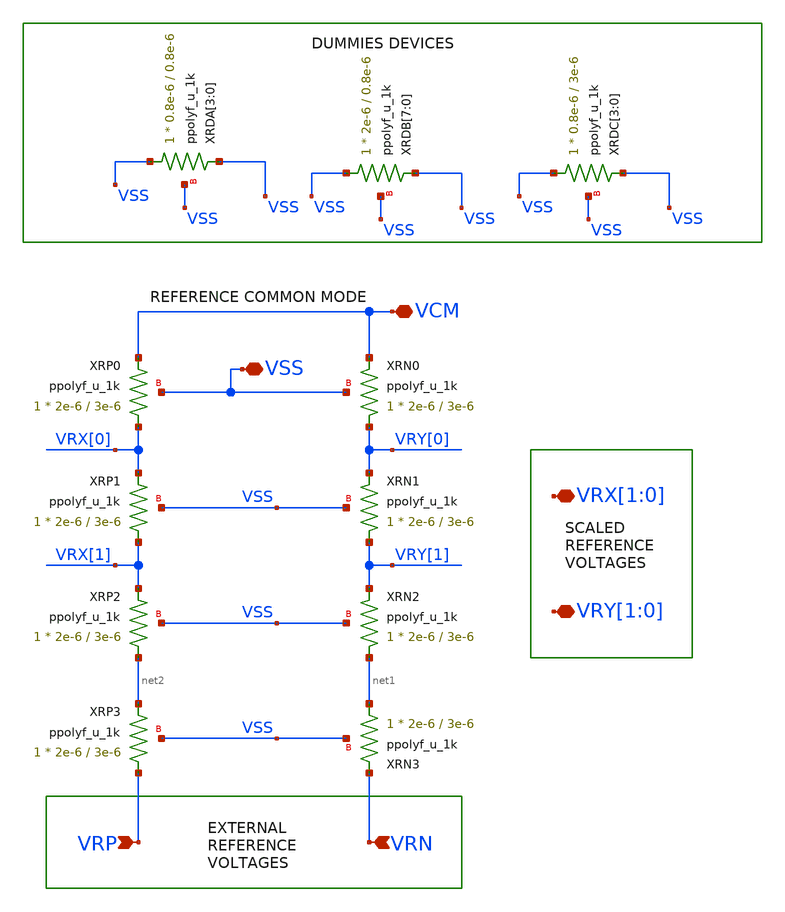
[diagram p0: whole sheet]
** sch_path: designs/sar_adc/dac/rdac/xschem/rdac.sch
**.subckt rdac VRN VRP VCM VRY[1],VRY[0] VRX[1],VRX[0] VSS
*.ipin VRN
*.ipin VRP
*.iopin VCM
*.iopin VRY[1],VRY[0]
*.iopin VRX[1],VRX[0]
*.iopin VSS
XRN0 VRY[0] VCM VSS ppolyf_u_1k r_width=2e-6 r_length=3e-6 m=1
XRN1 VRY[1] VRY[0] VSS ppolyf_u_1k r_width=2e-6 r_length=3e-6 m=1
XRN2 net1 VRY[1] VSS ppolyf_u_1k r_width=2e-6 r_length=3e-6 m=1
XRN3 net1 VRN VSS ppolyf_u_1k r_width=2e-6 r_length=3e-6 m=1
XRP0 VRX[0] VCM VSS ppolyf_u_1k r_width=2e-6 r_length=3e-6 m=1
XRP1 VRX[1] VRX[0] VSS ppolyf_u_1k r_width=2e-6 r_length=3e-6 m=1
XRP2 net2 VRX[1] VSS ppolyf_u_1k r_width=2e-6 r_length=3e-6 m=1
XRP3 VRP net2 VSS ppolyf_u_1k r_width=2e-6 r_length=3e-6 m=1
XRDC[3] VSS VSS VSS ppolyf_u_1k r_width=0.8e-6 r_length=3e-6 m=1
XRDC[2] VSS VSS VSS ppolyf_u_1k r_width=0.8e-6 r_length=3e-6 m=1
XRDC[1] VSS VSS VSS ppolyf_u_1k r_width=0.8e-6 r_length=3e-6 m=1
XRDC[0] VSS VSS VSS ppolyf_u_1k r_width=0.8e-6 r_length=3e-6 m=1
XRDB[7] VSS VSS VSS ppolyf_u_1k r_width=2e-6 r_length=0.8e-6 m=1
XRDB[6] VSS VSS VSS ppolyf_u_1k r_width=2e-6 r_length=0.8e-6 m=1
XRDB[5] VSS VSS VSS ppolyf_u_1k r_width=2e-6 r_length=0.8e-6 m=1
XRDB[4] VSS VSS VSS ppolyf_u_1k r_width=2e-6 r_length=0.8e-6 m=1
XRDB[3] VSS VSS VSS ppolyf_u_1k r_width=2e-6 r_length=0.8e-6 m=1
XRDB[2] VSS VSS VSS ppolyf_u_1k r_width=2e-6 r_length=0.8e-6 m=1
XRDB[1] VSS VSS VSS ppolyf_u_1k r_width=2e-6 r_length=0.8e-6 m=1
XRDB[0] VSS VSS VSS ppolyf_u_1k r_width=2e-6 r_length=0.8e-6 m=1
XRDA[3] VSS VSS VSS ppolyf_u_1k r_width=0.8e-6 r_length=0.8e-6 m=1
XRDA[2] VSS VSS VSS ppolyf_u_1k r_width=0.8e-6 r_length=0.8e-6 m=1
XRDA[1] VSS VSS VSS ppolyf_u_1k r_width=0.8e-6 r_length=0.8e-6 m=1
XRDA[0] VSS VSS VSS ppolyf_u_1k r_width=0.8e-6 r_length=0.8e-6 m=1
**.ends
.end
